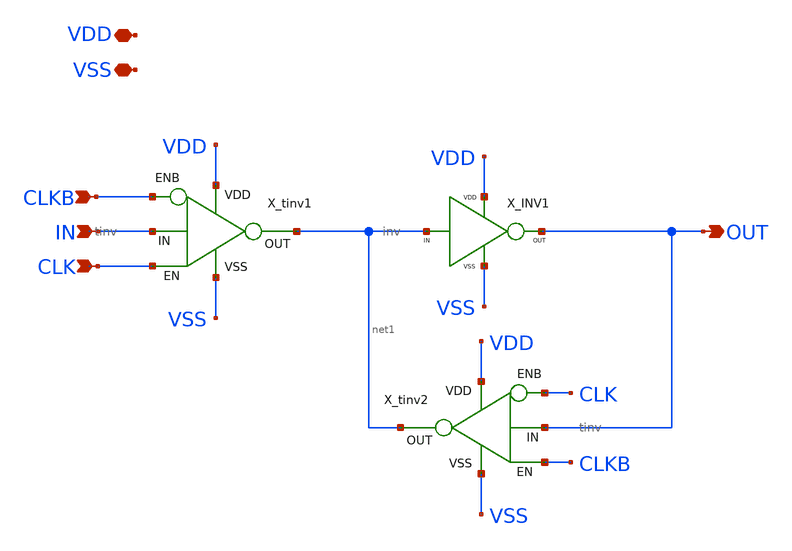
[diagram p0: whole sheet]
** sch_path: schem/latch.sch
**.subckt latch IN OUT CLK VDD VSS CLKB
*.ipin IN
*.opin OUT
*.ipin CLK
*.iopin VDD
*.iopin VSS
*.ipin CLKB
X_INV1 net1 OUT VDD VSS inv
X_tinv1 IN net1 VSS VDD CLK CLKB tinv
X_tinv2 OUT net1 VSS VDD CLKB CLK tinv
**.ends

* expanding   symbol:  inv.sym # of pins=4
** sym_path: schem/inv.sym
** sch_path: schem/inv.sch
.subckt inv X Y VDD VSS
*.ipin X
*.opin Y
*.iopin VDD
*.iopin VSS
XM1 Y X VSS GND sky130_fd_pr__nfet_01v8_lvt L=0.15 W=1.2 nf=1 ad='int((nf+1)/2) * W/nf * 0.29' as='int((nf+2)/2) * W/nf * 0.29'
+ pd='2*int((nf+1)/2) * (W/nf + 0.29)' ps='2*int((nf+2)/2) * (W/nf + 0.29)' nrd='0.29 / W' nrs='0.29 / W'
+ sa=0 sb=0 sd=0 mult=1 m=1
XM2 Y X VDD VDD sky130_fd_pr__pfet_01v8 L=0.15 W=1.6 nf=1 ad='int((nf+1)/2) * W/nf * 0.29' as='int((nf+2)/2) * W/nf * 0.29'
+ pd='2*int((nf+1)/2) * (W/nf + 0.29)' ps='2*int((nf+2)/2) * (W/nf + 0.29)' nrd='0.29 / W' nrs='0.29 / W'
+ sa=0 sb=0 sd=0 mult=1 m=1
.ends


* expanding   symbol:  tinv.sym # of pins=6
** sym_path: schem/tinv.sym
** sch_path: schem/tinv.sch
.subckt tinv X Y VSS VDD EN ENB
*.ipin X
*.opin Y
*.iopin VDD
*.iopin VSS
*.iopin EN
*.iopin ENB
XM1 net2 X VSS GND sky130_fd_pr__nfet_01v8_lvt L=0.15 W=1.2 nf=1 ad='int((nf+1)/2) * W/nf * 0.29' as='int((nf+2)/2) * W/nf * 0.29'
+ pd='2*int((nf+1)/2) * (W/nf + 0.29)' ps='2*int((nf+2)/2) * (W/nf + 0.29)' nrd='0.29 / W' nrs='0.29 / W'
+ sa=0 sb=0 sd=0 mult=1 m=1
XM2 net1 X VDD VDD sky130_fd_pr__pfet_01v8 L=0.15 W=1.6 nf=1 ad='int((nf+1)/2) * W/nf * 0.29' as='int((nf+2)/2) * W/nf * 0.29'
+ pd='2*int((nf+1)/2) * (W/nf + 0.29)' ps='2*int((nf+2)/2) * (W/nf + 0.29)' nrd='0.29 / W' nrs='0.29 / W'
+ sa=0 sb=0 sd=0 mult=1 m=1
XM3 Y ENB net1 VDD sky130_fd_pr__pfet_01v8 L=0.15 W=1.6 nf=1 ad='int((nf+1)/2) * W/nf * 0.29' as='int((nf+2)/2) * W/nf * 0.29'
+ pd='2*int((nf+1)/2) * (W/nf + 0.29)' ps='2*int((nf+2)/2) * (W/nf + 0.29)' nrd='0.29 / W' nrs='0.29 / W'
+ sa=0 sb=0 sd=0 mult=1 m=1
XM4 Y EN net2 GND sky130_fd_pr__nfet_01v8_lvt L=0.15 W=1.2 nf=1 ad='int((nf+1)/2) * W/nf * 0.29' as='int((nf+2)/2) * W/nf * 0.29'
+ pd='2*int((nf+1)/2) * (W/nf + 0.29)' ps='2*int((nf+2)/2) * (W/nf + 0.29)' nrd='0.29 / W' nrs='0.29 / W'
+ sa=0 sb=0 sd=0 mult=1 m=1
.ends

.end
